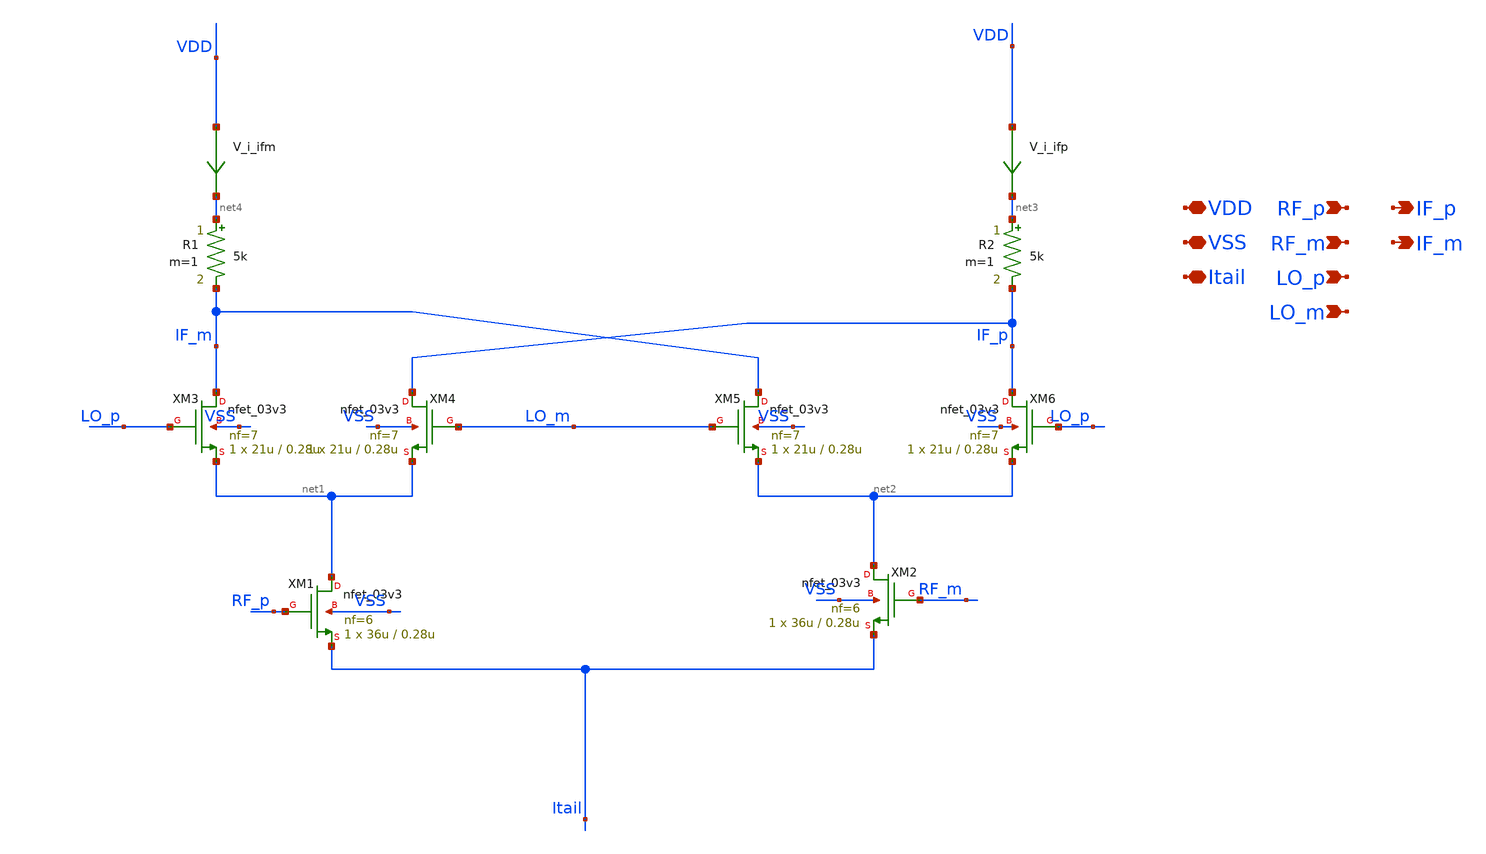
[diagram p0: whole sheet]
** sch_path: designs/mixer/schematic/Lei_mixer.sch
**.subckt Lei_mixer VDD LO_p LO_m Itail IF_m IF_p VSS RF_p RF_m
*.iopin VDD
*.ipin LO_p
*.ipin LO_m
*.iopin Itail
*.opin IF_m
*.opin IF_p
*.iopin VSS
*.ipin RF_p
*.ipin RF_m
XM1 net1 RF_p Itail VSS nfet_03v3 L=0.28u W=36u nf=6 ad='int((nf+1)/2) * W/nf * 0.18u' as='int((nf+2)/2) * W/nf * 0.18u'
+ pd='2*int((nf+1)/2) * (W/nf + 0.18u)' ps='2*int((nf+2)/2) * (W/nf + 0.18u)' nrd='0.18u / W' nrs='0.18u / W'
+ sa=0 sb=0 sd=0 m=1
XM2 net2 RF_m Itail VSS nfet_03v3 L=0.28u W=36u nf=6 ad='int((nf+1)/2) * W/nf * 0.18u' as='int((nf+2)/2) * W/nf * 0.18u'
+ pd='2*int((nf+1)/2) * (W/nf + 0.18u)' ps='2*int((nf+2)/2) * (W/nf + 0.18u)' nrd='0.18u / W' nrs='0.18u / W'
+ sa=0 sb=0 sd=0 m=1
XM3 IF_m LO_p net1 VSS nfet_03v3 L=0.28u W=21u nf=7 ad='int((nf+1)/2) * W/nf * 0.18u' as='int((nf+2)/2) * W/nf * 0.18u'
+ pd='2*int((nf+1)/2) * (W/nf + 0.18u)' ps='2*int((nf+2)/2) * (W/nf + 0.18u)' nrd='0.18u / W' nrs='0.18u / W'
+ sa=0 sb=0 sd=0 m=1
XM4 IF_p LO_m net1 VSS nfet_03v3 L=0.28u W=21u nf=7 ad='int((nf+1)/2) * W/nf * 0.18u' as='int((nf+2)/2) * W/nf * 0.18u'
+ pd='2*int((nf+1)/2) * (W/nf + 0.18u)' ps='2*int((nf+2)/2) * (W/nf + 0.18u)' nrd='0.18u / W' nrs='0.18u / W'
+ sa=0 sb=0 sd=0 m=1
XM5 IF_m LO_m net2 VSS nfet_03v3 L=0.28u W=21u nf=7 ad='int((nf+1)/2) * W/nf * 0.18u' as='int((nf+2)/2) * W/nf * 0.18u'
+ pd='2*int((nf+1)/2) * (W/nf + 0.18u)' ps='2*int((nf+2)/2) * (W/nf + 0.18u)' nrd='0.18u / W' nrs='0.18u / W'
+ sa=0 sb=0 sd=0 m=1
XM6 IF_p LO_p net2 VSS nfet_03v3 L=0.28u W=21u nf=7 ad='int((nf+1)/2) * W/nf * 0.18u' as='int((nf+2)/2) * W/nf * 0.18u'
+ pd='2*int((nf+1)/2) * (W/nf + 0.18u)' ps='2*int((nf+2)/2) * (W/nf + 0.18u)' nrd='0.18u / W' nrs='0.18u / W'
+ sa=0 sb=0 sd=0 m=1
R1 net4 IF_m 5k m=1
R2 net3 IF_p 5k m=1
V_i_ifm VDD net4 0
.save i(v_i_ifm)
V_i_ifp VDD net3 0
.save i(v_i_ifp)
**.ends
.end
